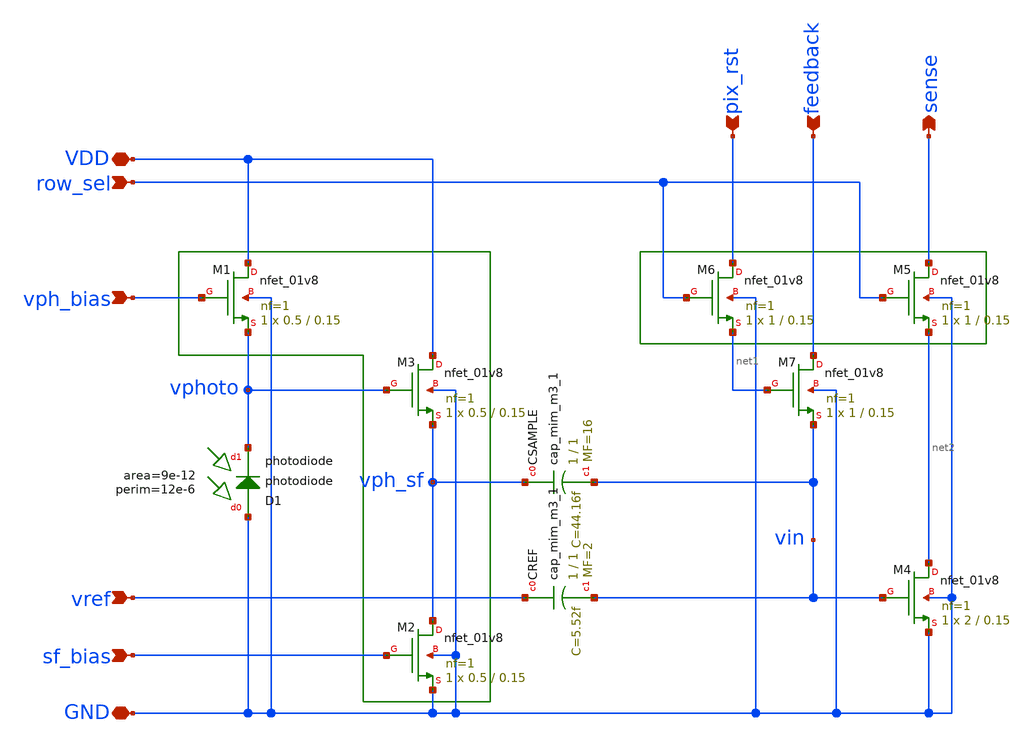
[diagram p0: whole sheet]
** sch_path: analog/xschem/openDVS_pedantic.sch
**.subckt openDVS_pedantic GND VDD row_sel vref vph_bias sf_bias pix_rst feedback sense
*.iopin GND
*.iopin VDD
*.ipin row_sel
*.ipin vref
*.ipin vph_bias
*.ipin sf_bias
*.ipin pix_rst
*.ipin feedback
*.opin sense
XCSAMPLE vph_sf vin sky130_fd_pr__cap_mim_m3_1 W=1 L=1 MF=16 m=16
XCREF vref vin sky130_fd_pr__cap_mim_m3_1 W=1 L=1 MF=2 m=2
XM1 VDD vph_bias vphoto GND sky130_fd_pr__nfet_01v8 L=0.15 W=0.5 nf=1 ad='int((1 + 1)/2) * 0.5 / 1 * 0.29'
+ as='int((1 + 2)/2) * 0.5 / 1 * 0.29' pd='2*int((1 + 1)/2) * (0.5 / 1 + 0.29)' ps='2*int((1 + 2)/2) * (0.5 / 1 + 0.29)'
+ nrd='0.29 / 0.5 ' nrs='0.29 / 0.5 ' sa=0 sb=0 sd=0 mult=1 m=1
XM4 net2 vin GND GND sky130_fd_pr__nfet_01v8 L=0.15 W=2 nf=1 ad='int((1 + 1)/2) * 2 / 1 * 0.29' as='int((1 + 2)/2) * 2 / 1 * 0.29'
+ pd='2*int((1 + 1)/2) * (2 / 1 + 0.29)' ps='2*int((1 + 2)/2) * (2 / 1 + 0.29)' nrd='0.29 / 2 ' nrs='0.29 / 2 '
+ sa=0 sb=0 sd=0 mult=1 m=1
XM7 feedback net1 vin GND sky130_fd_pr__nfet_01v8 L=0.15 W=1 nf=1 ad='int((1 + 1)/2) * 1 / 1 * 0.29'
+ as='int((1 + 2)/2) * 1 / 1 * 0.29' pd='2*int((1 + 1)/2) * (1 / 1 + 0.29)' ps='2*int((1 + 2)/2) * (1 / 1 + 0.29)'
+ nrd='0.29 / 1 ' nrs='0.29 / 1 ' sa=0 sb=0 sd=0 mult=1 m=1
XM2 vph_sf sf_bias GND GND sky130_fd_pr__nfet_01v8 L=0.15 W=0.5 nf=1 ad='int((1 + 1)/2) * 0.5 / 1 * 0.29'
+ as='int((1 + 2)/2) * 0.5 / 1 * 0.29' pd='2*int((1 + 1)/2) * (0.5 / 1 + 0.29)' ps='2*int((1 + 2)/2) * (0.5 / 1 + 0.29)'
+ nrd='0.29 / 0.5 ' nrs='0.29 / 0.5 ' sa=0 sb=0 sd=0 mult=1 m=1
XM3 VDD vphoto vph_sf GND sky130_fd_pr__nfet_01v8 L=0.15 W=0.5 nf=1 ad='int((1 + 1)/2) * 0.5 / 1 * 0.29'
+ as='int((1 + 2)/2) * 0.5 / 1 * 0.29' pd='2*int((1 + 1)/2) * (0.5 / 1 + 0.29)' ps='2*int((1 + 2)/2) * (0.5 / 1 + 0.29)'
+ nrd='0.29 / 0.5 ' nrs='0.29 / 0.5 ' sa=0 sb=0 sd=0 mult=1 m=1
XD1 GND vphoto sky130_fd_pr__photodiode area=9e-12 perim=12e-6
XM5 sense row_sel net2 GND sky130_fd_pr__nfet_01v8 L=0.15 W=1 nf=1 ad='int((1 + 1)/2) * 1 / 1 * 0.29'
+ as='int((1 + 2)/2) * 1 / 1 * 0.29' pd='2*int((1 + 1)/2) * (1 / 1 + 0.29)' ps='2*int((1 + 2)/2) * (1 / 1 + 0.29)'
+ nrd='0.29 / 1 ' nrs='0.29 / 1 ' sa=0 sb=0 sd=0 mult=1 m=1
XM6 pix_rst row_sel net1 GND sky130_fd_pr__nfet_01v8 L=0.15 W=1 nf=1 ad='int((1 + 1)/2) * 1 / 1 * 0.29'
+ as='int((1 + 2)/2) * 1 / 1 * 0.29' pd='2*int((1 + 1)/2) * (1 / 1 + 0.29)' ps='2*int((1 + 2)/2) * (1 / 1 + 0.29)'
+ nrd='0.29 / 1 ' nrs='0.29 / 1 ' sa=0 sb=0 sd=0 mult=1 m=1
**.ends
.end
